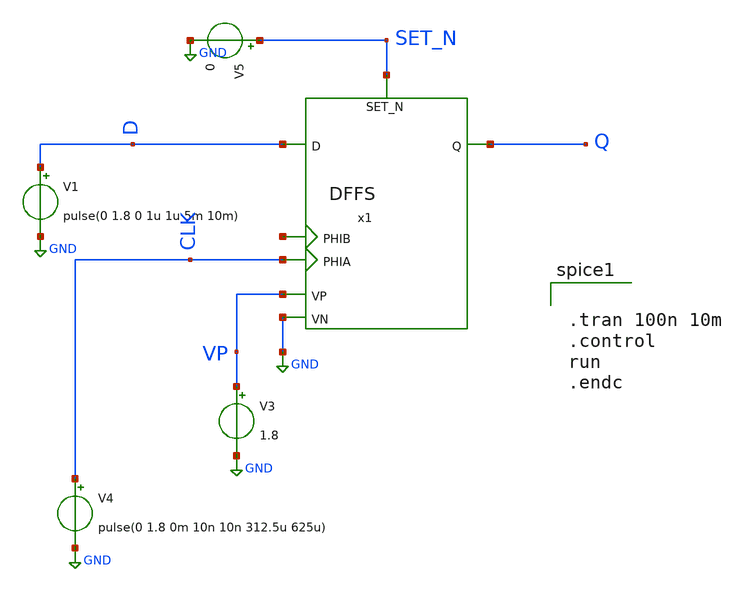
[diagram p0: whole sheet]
** sch_path: ADC/16bit_C2C/MagicAndSpice/EE431_FinalProj/DFFS_tb.sch
**.subckt DFFS_tb
V3 VP GND 1.8
V4 CLK GND pulse(0 1.8 0m 10n 10n 312.5u 625u)
V1 D GND pulse(0 1.8 0 1u 1u 5m 10m)
x1 CLK net1 D Q SET_N VP GND DFFS
V5 SET_N GND 0
**** begin user architecture code
 .lib $::SKYWATER_MODELS/sky130.lib.spice tt


.tran 100n 10m
.control
run
.endc

**** end user architecture code
**.ends
.GLOBAL GND
.end
